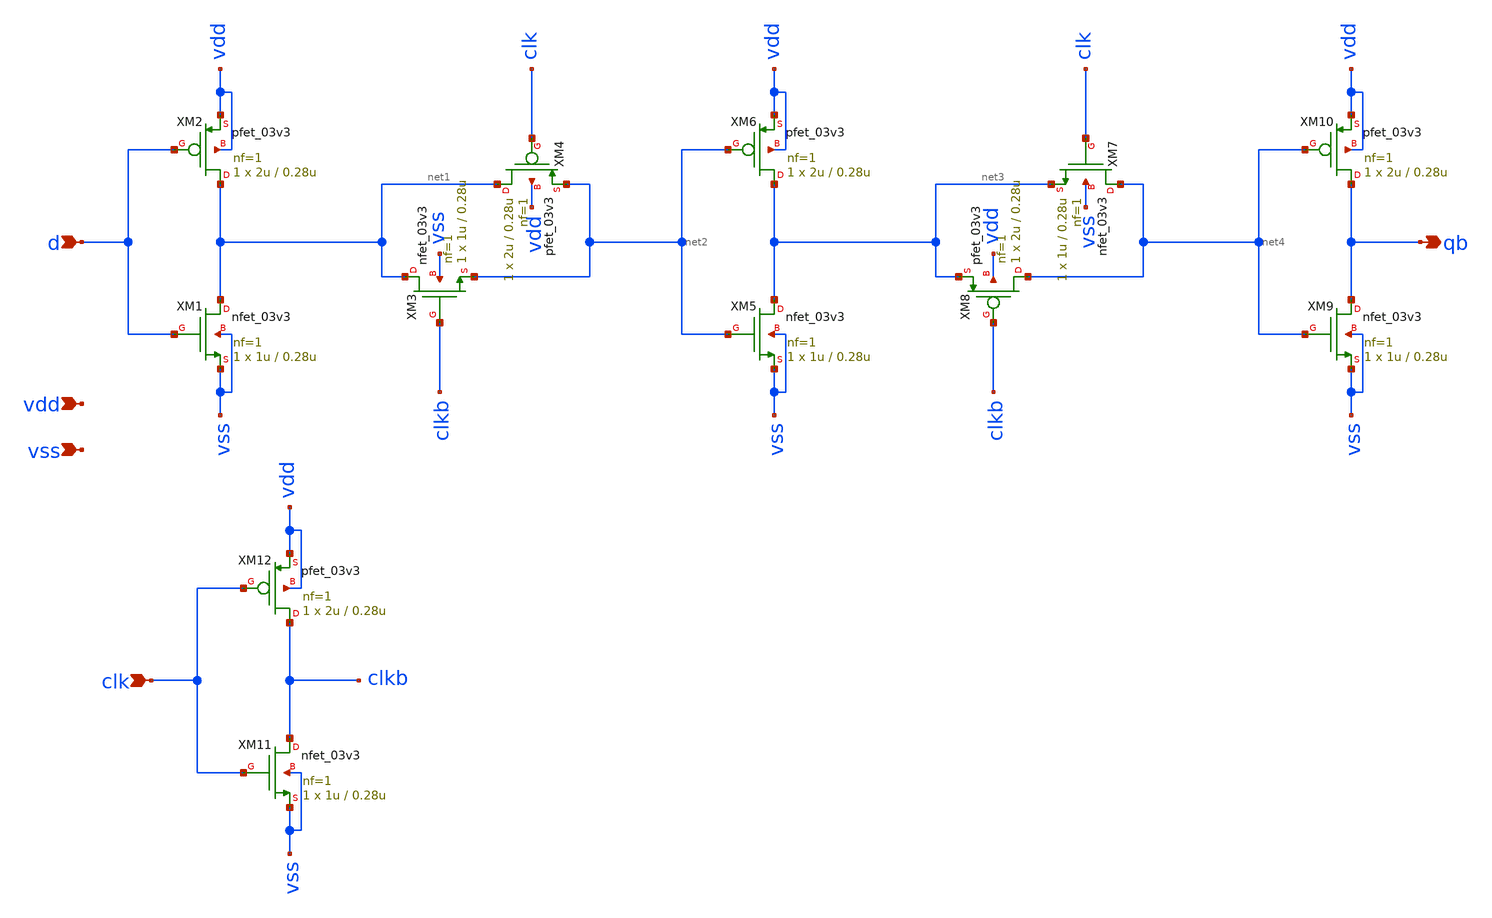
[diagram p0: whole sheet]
** sch_path: xschem/dff_dynamic.sch
**.subckt dff_dynamic d vdd vss clk qb
*.ipin d
*.ipin vdd
*.ipin vss
*.ipin clk
*.opin qb
XM1 net1 d vss vss nfet_03v3 L=0.28u W=1u nf=1 ad='int((nf+1)/2) * W/nf * 0.18u' as='int((nf+2)/2) * W/nf * 0.18u'
+ pd='2*int((nf+1)/2) * (W/nf + 0.18u)' ps='2*int((nf+2)/2) * (W/nf + 0.18u)' nrd='0.18u / W' nrs='0.18u / W'
+ sa=0 sb=0 sd=0 m=1
XM2 net1 d vdd vdd pfet_03v3 L=0.28u W=2u nf=1 ad='int((nf+1)/2) * W/nf * 0.18u' as='int((nf+2)/2) * W/nf * 0.18u'
+ pd='2*int((nf+1)/2) * (W/nf + 0.18u)' ps='2*int((nf+2)/2) * (W/nf + 0.18u)' nrd='0.18u / W' nrs='0.18u / W'
+ sa=0 sb=0 sd=0 m=1
XM3 net1 clkb net2 vss nfet_03v3 L=0.28u W=1u nf=1 ad='int((nf+1)/2) * W/nf * 0.18u' as='int((nf+2)/2) * W/nf * 0.18u'
+ pd='2*int((nf+1)/2) * (W/nf + 0.18u)' ps='2*int((nf+2)/2) * (W/nf + 0.18u)' nrd='0.18u / W' nrs='0.18u / W'
+ sa=0 sb=0 sd=0 m=1
XM4 net1 clk net2 vdd pfet_03v3 L=0.28u W=2u nf=1 ad='int((nf+1)/2) * W/nf * 0.18u' as='int((nf+2)/2) * W/nf * 0.18u'
+ pd='2*int((nf+1)/2) * (W/nf + 0.18u)' ps='2*int((nf+2)/2) * (W/nf + 0.18u)' nrd='0.18u / W' nrs='0.18u / W'
+ sa=0 sb=0 sd=0 m=1
XM5 net3 net2 vss vss nfet_03v3 L=0.28u W=1u nf=1 ad='int((nf+1)/2) * W/nf * 0.18u' as='int((nf+2)/2) * W/nf * 0.18u'
+ pd='2*int((nf+1)/2) * (W/nf + 0.18u)' ps='2*int((nf+2)/2) * (W/nf + 0.18u)' nrd='0.18u / W' nrs='0.18u / W'
+ sa=0 sb=0 sd=0 m=1
XM6 net3 net2 vdd vdd pfet_03v3 L=0.28u W=2u nf=1 ad='int((nf+1)/2) * W/nf * 0.18u' as='int((nf+2)/2) * W/nf * 0.18u'
+ pd='2*int((nf+1)/2) * (W/nf + 0.18u)' ps='2*int((nf+2)/2) * (W/nf + 0.18u)' nrd='0.18u / W' nrs='0.18u / W'
+ sa=0 sb=0 sd=0 m=1
XM7 net4 clk net3 vss nfet_03v3 L=0.28u W=1u nf=1 ad='int((nf+1)/2) * W/nf * 0.18u' as='int((nf+2)/2) * W/nf * 0.18u'
+ pd='2*int((nf+1)/2) * (W/nf + 0.18u)' ps='2*int((nf+2)/2) * (W/nf + 0.18u)' nrd='0.18u / W' nrs='0.18u / W'
+ sa=0 sb=0 sd=0 m=1
XM8 net4 clkb net3 vdd pfet_03v3 L=0.28u W=2u nf=1 ad='int((nf+1)/2) * W/nf * 0.18u' as='int((nf+2)/2) * W/nf * 0.18u'
+ pd='2*int((nf+1)/2) * (W/nf + 0.18u)' ps='2*int((nf+2)/2) * (W/nf + 0.18u)' nrd='0.18u / W' nrs='0.18u / W'
+ sa=0 sb=0 sd=0 m=1
XM9 qb net4 vss vss nfet_03v3 L=0.28u W=1u nf=1 ad='int((nf+1)/2) * W/nf * 0.18u' as='int((nf+2)/2) * W/nf * 0.18u'
+ pd='2*int((nf+1)/2) * (W/nf + 0.18u)' ps='2*int((nf+2)/2) * (W/nf + 0.18u)' nrd='0.18u / W' nrs='0.18u / W'
+ sa=0 sb=0 sd=0 m=1
XM10 qb net4 vdd vdd pfet_03v3 L=0.28u W=2u nf=1 ad='int((nf+1)/2) * W/nf * 0.18u' as='int((nf+2)/2) * W/nf * 0.18u'
+ pd='2*int((nf+1)/2) * (W/nf + 0.18u)' ps='2*int((nf+2)/2) * (W/nf + 0.18u)' nrd='0.18u / W' nrs='0.18u / W'
+ sa=0 sb=0 sd=0 m=1
XM11 clkb clk vss vss nfet_03v3 L=0.28u W=1u nf=1 ad='int((nf+1)/2) * W/nf * 0.18u' as='int((nf+2)/2) * W/nf * 0.18u'
+ pd='2*int((nf+1)/2) * (W/nf + 0.18u)' ps='2*int((nf+2)/2) * (W/nf + 0.18u)' nrd='0.18u / W' nrs='0.18u / W'
+ sa=0 sb=0 sd=0 m=1
XM12 clkb clk vdd vdd pfet_03v3 L=0.28u W=2u nf=1 ad='int((nf+1)/2) * W/nf * 0.18u' as='int((nf+2)/2) * W/nf * 0.18u'
+ pd='2*int((nf+1)/2) * (W/nf + 0.18u)' ps='2*int((nf+2)/2) * (W/nf + 0.18u)' nrd='0.18u / W' nrs='0.18u / W'
+ sa=0 sb=0 sd=0 m=1
**.ends
.end
